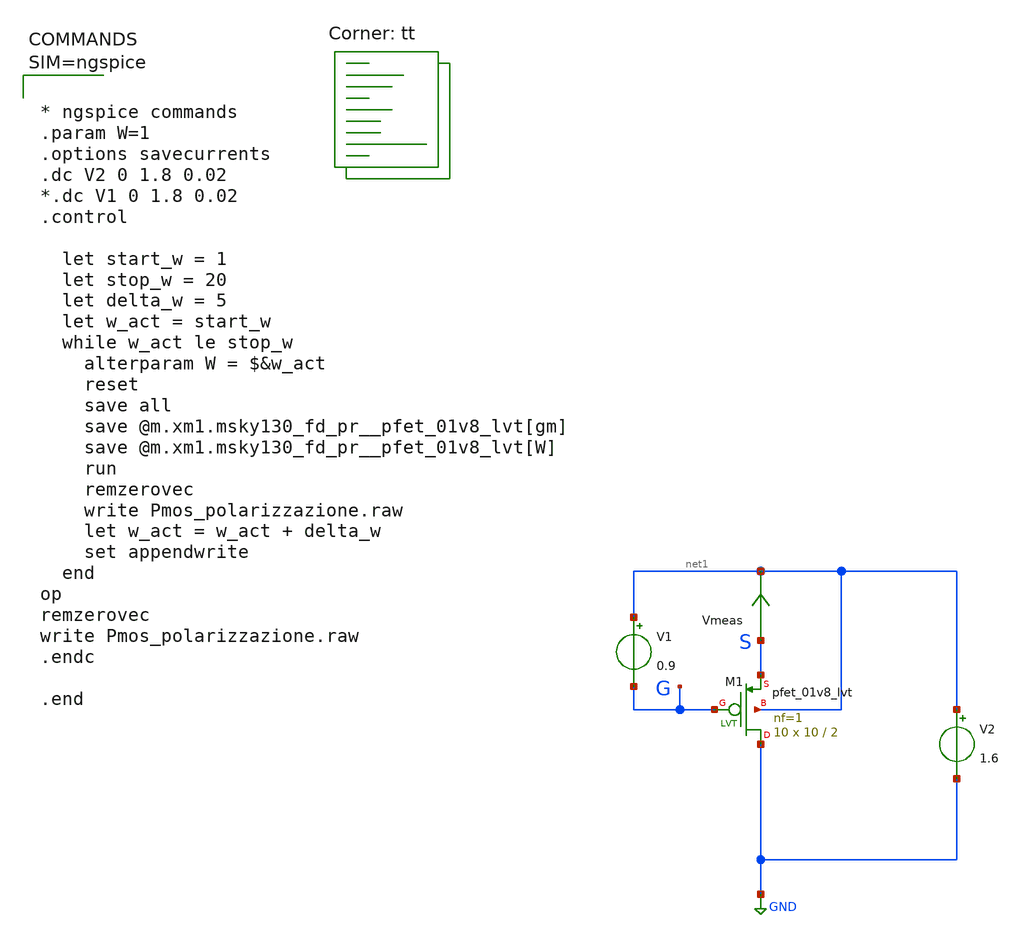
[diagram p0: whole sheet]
** sch_path: xschem/Pmos_polarizzazione.sch
**.subckt Pmos_polarizzazione
V2 net1 GND 1.6
V1 net1 G 0.9
Vmeas S net1 0
.save i(vmeas)
XM1 GND G S net1 sky130_fd_pr__pfet_01v8_lvt L=2 W=10 nf=1 ad='int((nf+1)/2) * W/nf * 0.29' as='int((nf+2)/2) * W/nf * 0.29'
+ pd='2*int((nf+1)/2) * (W/nf + 0.29)' ps='2*int((nf+2)/2) * (W/nf + 0.29)' nrd='0.29 / W' nrs='0.29 / W'
+ sa=0 sb=0 sd=0 mult=10 m=10
**** begin user architecture code
.lib $::SKYWATER_MODELS/sky130.lib.spice tt



* ngspice commands
.param W=1
.options savecurrents
.dc V2 0 1.8 0.02
*.dc V1 0 1.8 0.02
.control

  let start_w = 1
  let stop_w = 20
  let delta_w = 5
  let w_act = start_w
  while w_act le stop_w
    alterparam W = $&w_act
    reset
    save all
    save @m.xm1.msky130_fd_pr__pfet_01v8_lvt[gm]
    save @m.xm1.msky130_fd_pr__pfet_01v8_lvt[W]
    run
    remzerovec
    write Pmos_polarizzazione.raw
    let w_act = w_act + delta_w
    set appendwrite
  end
op
remzerovec
write Pmos_polarizzazione.raw
.endc

.end



**** end user architecture code
**.ends
.GLOBAL GND
.end
